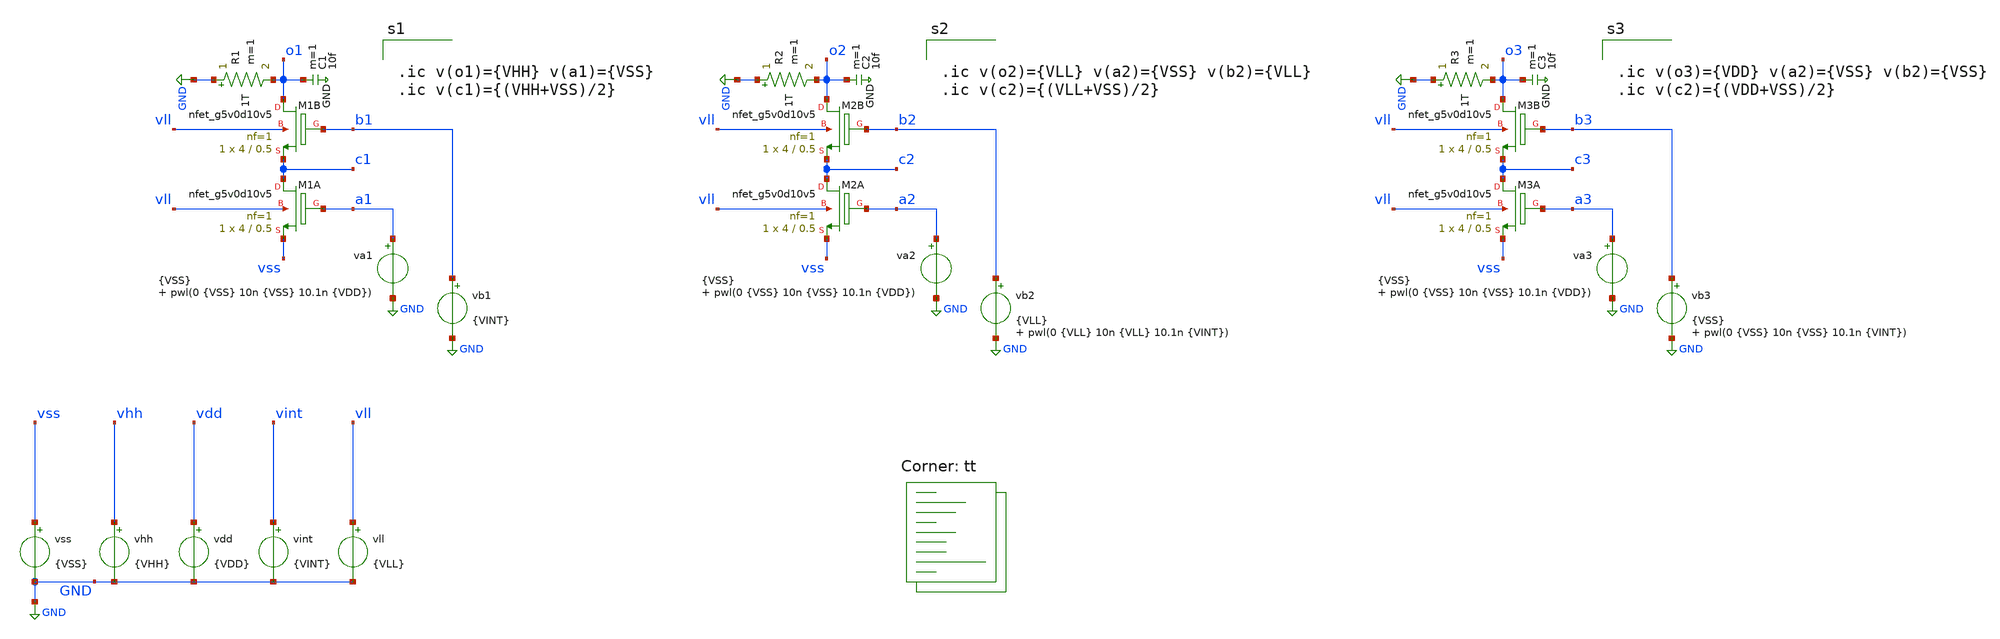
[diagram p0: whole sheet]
** sch_path: test-hvswcases.sch
**.subckt test-hvswcases
vhh vhh GND {VHH}
vint vint GND {VINT}
vll vll GND {VLL}
vb1 b1 GND {VINT}
vdd vdd GND {VDD}
va1 a1 GND {VSS} pwl(0 {VSS} 10n {VSS} 10.1n {VDD})
XM1A c1 a1 vss vll sky130_fd_pr__nfet_g5v0d10v5 L=0.5 W=4 nf=1 ad='int((nf+1)/2) * W/nf * 0.29' as='int((nf+2)/2) * W/nf * 0.29'
+ pd='2*int((nf+1)/2) * (W/nf + 0.29)' ps='2*int((nf+2)/2) * (W/nf + 0.29)' nrd='0.29 / W' nrs='0.29 / W'
+ sa=0 sb=0 sd=0 mult=1 m=1
XM1B o1 b1 c1 vll sky130_fd_pr__nfet_g5v0d10v5 L=0.5 W=4 nf=1 ad='int((nf+1)/2) * W/nf * 0.29' as='int((nf+2)/2) * W/nf * 0.29'
+ pd='2*int((nf+1)/2) * (W/nf + 0.29)' ps='2*int((nf+2)/2) * (W/nf + 0.29)' nrd='0.29 / W' nrs='0.29 / W'
+ sa=0 sb=0 sd=0 mult=1 m=1
R1 GND o1 1T m=1
vss vss GND {VSS}
vb2 b2 GND {VLL} pwl(0 {VLL} 10n {VLL} 10.1n {VINT})
va2 a2 GND {VSS} pwl(0 {VSS} 10n {VSS} 10.1n {VDD})
XM2A c2 a2 vss vll sky130_fd_pr__nfet_g5v0d10v5 L=0.5 W=4 nf=1 ad='int((nf+1)/2) * W/nf * 0.29' as='int((nf+2)/2) * W/nf * 0.29'
+ pd='2*int((nf+1)/2) * (W/nf + 0.29)' ps='2*int((nf+2)/2) * (W/nf + 0.29)' nrd='0.29 / W' nrs='0.29 / W'
+ sa=0 sb=0 sd=0 mult=1 m=1
XM2B o2 b2 c2 vll sky130_fd_pr__nfet_g5v0d10v5 L=0.5 W=4 nf=1 ad='int((nf+1)/2) * W/nf * 0.29' as='int((nf+2)/2) * W/nf * 0.29'
+ pd='2*int((nf+1)/2) * (W/nf + 0.29)' ps='2*int((nf+2)/2) * (W/nf + 0.29)' nrd='0.29 / W' nrs='0.29 / W'
+ sa=0 sb=0 sd=0 mult=1 m=1
R2 GND o2 1T m=1
C1 o1 GND 10f m=1
C2 o2 GND 10f m=1
vb3 b3 GND {VSS} pwl(0 {VSS} 10n {VSS} 10.1n {VINT})
va3 a3 GND {VSS} pwl(0 {VSS} 10n {VSS} 10.1n {VDD})
XM3A c3 a3 vss vll sky130_fd_pr__nfet_g5v0d10v5 L=0.5 W=4 nf=1 ad='int((nf+1)/2) * W/nf * 0.29' as='int((nf+2)/2) * W/nf * 0.29'
+ pd='2*int((nf+1)/2) * (W/nf + 0.29)' ps='2*int((nf+2)/2) * (W/nf + 0.29)' nrd='0.29 / W' nrs='0.29 / W'
+ sa=0 sb=0 sd=0 mult=1 m=1
XM3B o3 b3 c3 vll sky130_fd_pr__nfet_g5v0d10v5 L=0.5 W=4 nf=1 ad='int((nf+1)/2) * W/nf * 0.29' as='int((nf+2)/2) * W/nf * 0.29'
+ pd='2*int((nf+1)/2) * (W/nf + 0.29)' ps='2*int((nf+2)/2) * (W/nf + 0.29)' nrd='0.29 / W' nrs='0.29 / W'
+ sa=0 sb=0 sd=0 mult=1 m=1
R3 GND o3 1T m=1
C3 o3 GND 10f m=1
**** begin user architecture code
.lib $::SKYWATER_MODELS/sky130.lib.spice tt



.param VLL=-3.8
.param VDD=1.8
.param VSS=0
.param VLH=0
.param VHH=6.7
.param VINT={(VHH+VLL)/2}
.option savecurrents
.control
  save all
  op
  remzerovec
  write test-hvswcases.raw
  set appendwrite
  tran 100p 20n uic
  remzerovec
  write test-hvswcases.raw
.endc





.ic v(o1)={VHH} v(a1)={VSS}
.ic v(c1)={(VHH+VSS)/2}




.ic v(o2)={VLL} v(a2)={VSS} v(b2)={VLL}
.ic v(c2)={(VLL+VSS)/2}




.ic v(o3)={VDD} v(a2)={VSS} v(b2)={VSS}
.ic v(c2)={(VDD+VSS)/2}


**** end user architecture code
**.ends
.GLOBAL GND
.end
